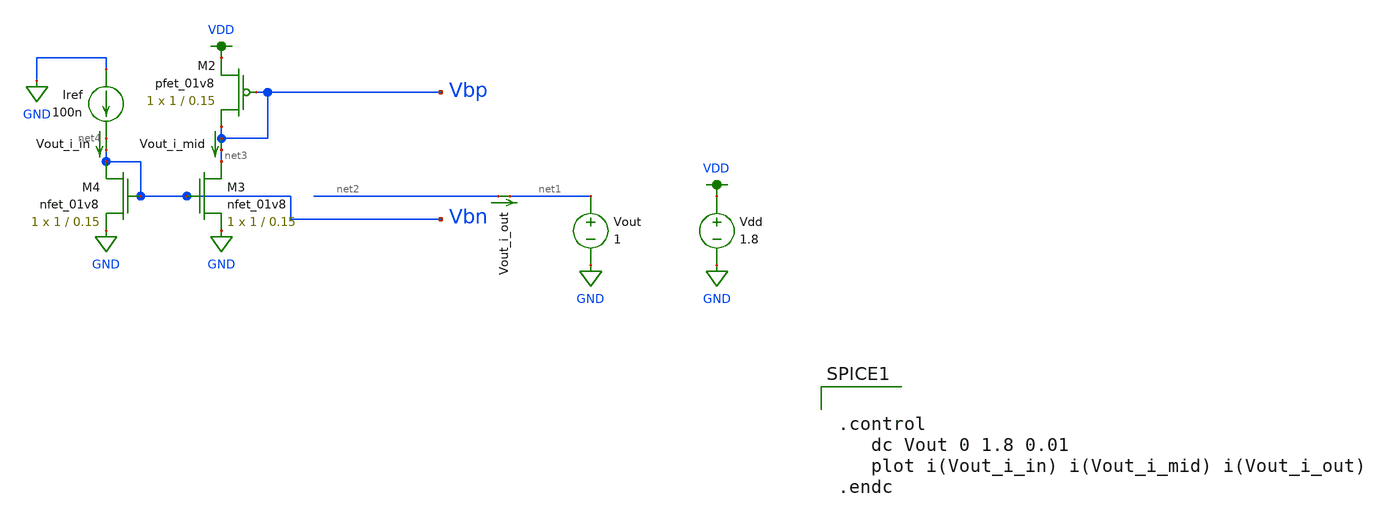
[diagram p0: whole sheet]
** sch_path: test_harness_current_mirror.sch
**.subckt test_harness_current_mirror
Vout net1 GND 1
Iref GND net4 100n
XM2 Vbp Vbp VDD VDD sky130_fd_pr__pfet_01v8 L=0.15 W=1 nf=1 ad='int((nf+1)/2) * W/nf * 0.29' as='int((nf+2)/2) * W/nf * 0.29'
+ pd='2*int((nf+1)/2) * (W/nf + 0.29)' ps='2*int((nf+2)/2) * (W/nf + 0.29)' nrd='0.29 / W' nrs='0.29 / W'
+ sa=0 sb=0 sd=0 mult=1 m=1
XM3 net3 Vbn GND GND sky130_fd_pr__nfet_01v8 L=0.15 W=1 nf=1 ad='int((nf+1)/2) * W/nf * 0.29' as='int((nf+2)/2) * W/nf * 0.29'
+ pd='2*int((nf+1)/2) * (W/nf + 0.29)' ps='2*int((nf+2)/2) * (W/nf + 0.29)' nrd='0.29 / W' nrs='0.29 / W'
+ sa=0 sb=0 sd=0 mult=1 m=1
XM4 Vbn Vbn GND GND sky130_fd_pr__nfet_01v8 L=0.15 W=1 nf=1 ad='int((nf+1)/2) * W/nf * 0.29' as='int((nf+2)/2) * W/nf * 0.29'
+ pd='2*int((nf+1)/2) * (W/nf + 0.29)' ps='2*int((nf+2)/2) * (W/nf + 0.29)' nrd='0.29 / W' nrs='0.29 / W'
+ sa=0 sb=0 sd=0 mult=1 m=1
Vout_i_in net4 Vbn 0
.save i(vout_i_in)
Vout_i_mid Vbp net3 0
.save i(vout_i_mid)
Vout_i_out net2 net1 0
.save i(vout_i_out)
Vdd VDD GND 1.8
**** begin user architecture code


.control
   dc Vout 0 1.8 0.01
   plot i(Vout_i_in) i(Vout_i_mid) i(Vout_i_out)
.endc


.option wnflag=1
.param MC_SWITCH=0.0
.lib ~/skywater/skywater-pdk/libraries/sky130_fd_pr_ngspice/latest/models/sky130.lib.spice tt

**** end user architecture code
**.ends
.GLOBAL GND
.GLOBAL VDD
.end
